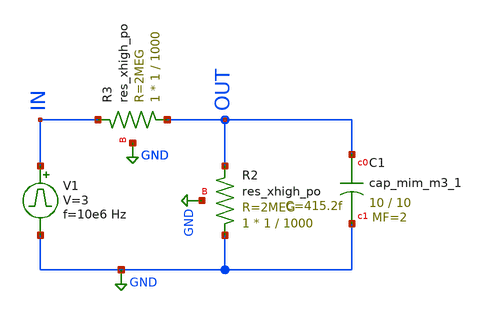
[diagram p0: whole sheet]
** sch_path: test.sch
**.subckt test
XC1 OUT GND sky130_fd_pr__cap_mim_m3_1 W=10 L=10 MF=2 m=2
V1 IN GND pulse 0 3 '0.495/ 10e6 ' '0.01/10e6 ' '0.01/10e6 ' '0.49/10e6 ' '1/10e6 '
XR2 GND OUT GND sky130_fd_pr__res_xhigh_po W=1 L=1000 mult=1 m=1
XR3 OUT IN GND sky130_fd_pr__res_xhigh_po W=1 L=1000 mult=1 m=1
**** begin user architecture code

.include $::SKYWATER_MODELS/cells/nfet_01v8/sky130_fd_pr__nfet_01v8__tt.corner.spice
.include $::SKYWATER_MODELS/cells/nfet_01v8_lvt/sky130_fd_pr__nfet_01v8_lvt__tt.corner.spice
.include $::SKYWATER_MODELS/cells/pfet_01v8/sky130_fd_pr__pfet_01v8__tt.corner.spice
.include $::SKYWATER_MODELS/cells/nfet_03v3_nvt/sky130_fd_pr__nfet_03v3_nvt__tt.corner.spice
.include $::SKYWATER_MODELS/cells/nfet_05v0_nvt/sky130_fd_pr__nfet_05v0_nvt__tt.corner.spice
.include $::SKYWATER_MODELS/cells/esd_nfet_01v8/sky130_fd_pr__esd_nfet_01v8__tt.corner.spice
.include $::SKYWATER_MODELS/cells/pfet_01v8_lvt/sky130_fd_pr__pfet_01v8_lvt__tt.corner.spice
.include $::SKYWATER_MODELS/cells/pfet_01v8_hvt/sky130_fd_pr__pfet_01v8_hvt__tt.corner.spice
.include $::SKYWATER_MODELS/cells/esd_pfet_g5v0d10v5/sky130_fd_pr__esd_pfet_g5v0d10v5__tt.corner.spice
.include $::SKYWATER_MODELS/cells/pfet_g5v0d10v5/sky130_fd_pr__pfet_g5v0d10v5__tt.corner.spice
.include $::SKYWATER_MODELS/cells/pfet_g5v0d16v0/sky130_fd_pr__pfet_g5v0d16v0__tt.corner.spice
.include $::SKYWATER_MODELS/cells/nfet_g5v0d10v5/sky130_fd_pr__nfet_g5v0d10v5__tt.corner.spice
.include $::SKYWATER_MODELS/cells/nfet_g5v0d16v0/sky130_fd_pr__nfet_g5v0d16v0__tt_discrete.corner.spice
.include $::SKYWATER_MODELS/cells/esd_nfet_g5v0d10v5/sky130_fd_pr__esd_nfet_g5v0d10v5__tt.corner.spice
.include $::SKYWATER_MODELS/models/corners/tt/nonfet.spice
* Mismatch parameters
.include $::SKYWATER_MODELS/cells/nfet_01v8/sky130_fd_pr__nfet_01v8__mismatch.corner.spice
.include $::SKYWATER_MODELS/cells/pfet_01v8/sky130_fd_pr__pfet_01v8__mismatch.corner.spice
.include $::SKYWATER_MODELS/cells/nfet_01v8_lvt/sky130_fd_pr__nfet_01v8_lvt__mismatch.corner.spice
.include $::SKYWATER_MODELS/cells/pfet_01v8_lvt/sky130_fd_pr__pfet_01v8_lvt__mismatch.corner.spice
.include $::SKYWATER_MODELS/cells/pfet_01v8_hvt/sky130_fd_pr__pfet_01v8_hvt__mismatch.corner.spice
.include $::SKYWATER_MODELS/cells/nfet_g5v0d10v5/sky130_fd_pr__nfet_g5v0d10v5__mismatch.corner.spice
.include $::SKYWATER_MODELS/cells/pfet_g5v0d10v5/sky130_fd_pr__pfet_g5v0d10v5__mismatch.corner.spice
.include $::SKYWATER_MODELS/cells/nfet_05v0_nvt/sky130_fd_pr__nfet_05v0_nvt__mismatch.corner.spice
.include $::SKYWATER_MODELS/cells/nfet_03v3_nvt/sky130_fd_pr__nfet_03v3_nvt__mismatch.corner.spice
* Resistor$::SKYWATER_MODELS/Capacitor
.include $::SKYWATER_MODELS/models/r+c/res_typical__cap_typical.spice
.include $::SKYWATER_MODELS/models/r+c/res_typical__cap_typical__lin.spice
* Special cells
.include $::SKYWATER_MODELS/models/corners/tt/specialized_cells.spice
* All models
.include $::SKYWATER_MODELS/models/all.spice
* Corner
.include $::SKYWATER_MODELS/models/corners/tt/rf.spice



.save all
.control
tran 1n 1u uic
plot out
.endc


**** end user architecture code
**.ends
.GLOBAL GND
.end
